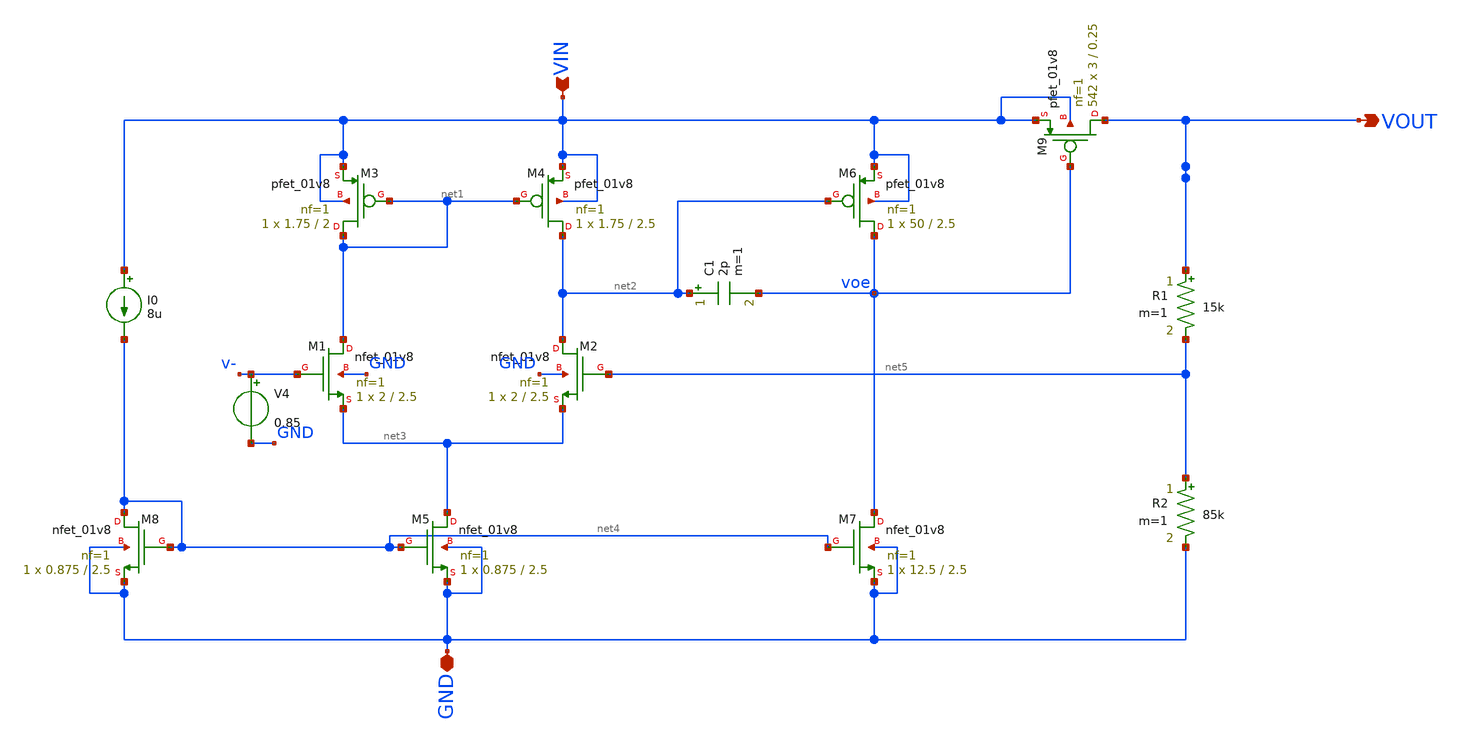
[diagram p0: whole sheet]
** sch_path: xschem/UREx-LDO-v1.sch
**.subckt UREx-LDO-v1 VIN VOUT GND
*.ipin VIN
*.opin VOUT
*.iopin GND
XM1 net1 v- net3 GND sky130_fd_pr__nfet_01v8 L=2.5 W=2 nf=1 ad='int((1 + 1)/2) * 2 / 1 * 0.29' as='int((1 + 2)/2) * 2 / 1 * 0.29'
+ pd='2*int((1 + 1)/2) * (2 / 1 + 0.29)' ps='2*int((1 + 2)/2) * (2 / 1 + 0.29)' nrd='0.29 / 2 ' nrs='0.29 / 2 '
+ sa=0 sb=0 sd=0 mult=1 m=1
XM3 net1 net1 VIN VIN sky130_fd_pr__pfet_01v8 L=2 W=1.75 nf=1 ad='int((1 + 1)/2) * 1.75 / 1 * 0.29' as='int((1 + 2)/2) * 1.75 / 1 * 0.29'
+ pd='2*int((1 + 1)/2) * (1.75 / 1 + 0.29)' ps='2*int((1 + 2)/2) * (1.75 / 1 + 0.29)' nrd='0.29 / 1.75 '
+ nrs='0.29 / 1.75 ' sa=0 sb=0 sd=0 mult=1 m=1
XM2 net2 net5 net3 GND sky130_fd_pr__nfet_01v8 L=2.5 W=2 nf=1 ad='int((1 + 1)/2) * 2 / 1 * 0.29' as='int((1 + 2)/2) * 2 / 1 * 0.29'
+ pd='2*int((1 + 1)/2) * (2 / 1 + 0.29)' ps='2*int((1 + 2)/2) * (2 / 1 + 0.29)' nrd='0.29 / 2 ' nrs='0.29 / 2 '
+ sa=0 sb=0 sd=0 mult=1 m=1
XM4 net2 net1 VIN VIN sky130_fd_pr__pfet_01v8 L=2.5 W=1.75 nf=1 ad='int((1 + 1)/2) * 1.75 / 1 * 0.29'
+ as='int((1 + 2)/2) * 1.75 / 1 * 0.29' pd='2*int((1 + 1)/2) * (1.75 / 1 + 0.29)' ps='2*int((1 + 2)/2) * (1.75 / 1 + 0.29)'
+ nrd='0.29 / 1.75 ' nrs='0.29 / 1.75 ' sa=0 sb=0 sd=0 mult=1 m=1
XM6 voe net2 VIN VIN sky130_fd_pr__pfet_01v8 L=2.5 W=50 nf=1 ad='int((1 + 1)/2) * 50 / 1 * 0.29' as='int((1 + 2)/2) * 50 / 1 * 0.29'
+ pd='2*int((1 + 1)/2) * (50 / 1 + 0.29)' ps='2*int((1 + 2)/2) * (50 / 1 + 0.29)' nrd='0.29 / 50 ' nrs='0.29 / 50 '
+ sa=0 sb=0 sd=0 mult=1 m=1
XM5 net3 net4 GND GND sky130_fd_pr__nfet_01v8 L=2.5 W=0.875 nf=1 ad='int((1 + 1)/2) * 0.875 / 1 * 0.29'
+ as='int((1 + 2)/2) * 0.875 / 1 * 0.29' pd='2*int((1 + 1)/2) * (0.875 / 1 + 0.29)' ps='2*int((1 + 2)/2) * (0.875 / 1 + 0.29)'
+ nrd='0.29 / 0.875 ' nrs='0.29 / 0.875 ' sa=0 sb=0 sd=0 mult=1 m=1
XM7 voe net4 GND GND sky130_fd_pr__nfet_01v8 L=2.5 W=12.5 nf=1 ad='int((1 + 1)/2) * 12.5 / 1 * 0.29'
+ as='int((1 + 2)/2) * 12.5 / 1 * 0.29' pd='2*int((1 + 1)/2) * (12.5 / 1 + 0.29)' ps='2*int((1 + 2)/2) * (12.5 / 1 + 0.29)'
+ nrd='0.29 / 12.5 ' nrs='0.29 / 12.5 ' sa=0 sb=0 sd=0 mult=1 m=1
XM8 net4 net4 GND GND sky130_fd_pr__nfet_01v8 L=2.5 W=0.875 nf=1 ad='int((1 + 1)/2) * 0.875 / 1 * 0.29'
+ as='int((1 + 2)/2) * 0.875 / 1 * 0.29' pd='2*int((1 + 1)/2) * (0.875 / 1 + 0.29)' ps='2*int((1 + 2)/2) * (0.875 / 1 + 0.29)'
+ nrd='0.29 / 0.875 ' nrs='0.29 / 0.875 ' sa=0 sb=0 sd=0 mult=1 m=1
C1 net2 voe 2p m=1
I0 VIN net4 8u
R1 VOUT net5 15k m=1
R2 net5 GND 85k m=1
V4 v- GND 0.85
XM9 VOUT voe VIN VIN sky130_fd_pr__pfet_01v8 L=0.25 W=3 nf=1 ad='int((1 + 1)/2) * 3 / 1 * 0.29' as='int((1 + 2)/2) * 3 / 1 * 0.29'
+ pd='2*int((1 + 1)/2) * (3 / 1 + 0.29)' ps='2*int((1 + 2)/2) * (3 / 1 + 0.29)' nrd='0.29 / 3 ' nrs='0.29 / 3 '
+ sa=0 sb=0 sd=0 mult=542 m=542
**.ends
.end
